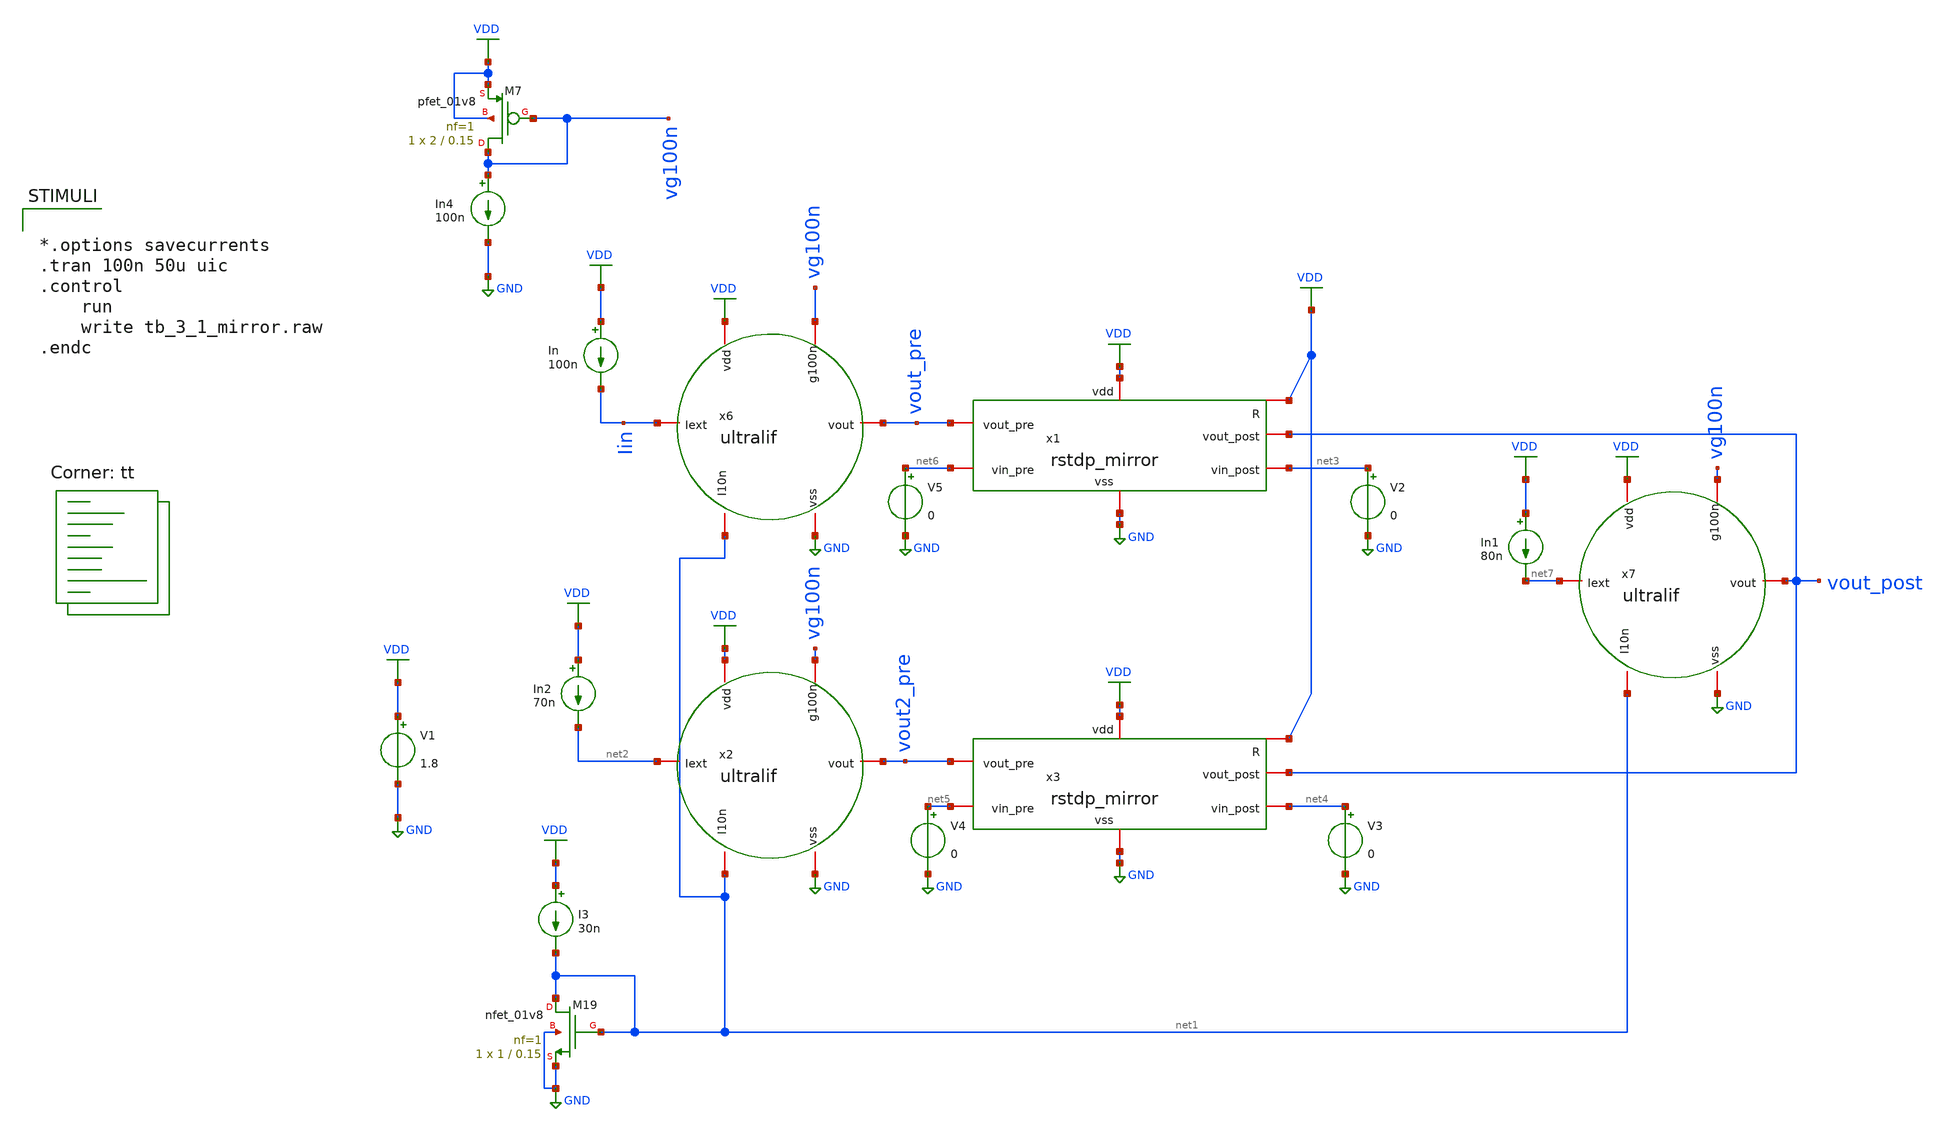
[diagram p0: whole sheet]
** sch_path: tb_3_1_mirror.sch
**.subckt tb_3_1_mirror
V1 VDD GND 1.8
x6 VDD Iin vout_pre net1 GND vg100n ultralif
x7 VDD net7 vout_post net1 GND vg100n ultralif
XM19 net1 net1 GND GND sky130_fd_pr__nfet_01v8 L=0.15 W=1 nf=1 ad='int((nf+1)/2) * W/nf * 0.29' as='int((nf+2)/2) * W/nf * 0.29'
+ pd='2*int((nf+1)/2) * (W/nf + 0.29)' ps='2*int((nf+2)/2) * (W/nf + 0.29)' nrd='0.29 / W' nrs='0.29 / W'
+ sa=0 sb=0 sd=0 mult=1 m=1
I3 VDD net1 30n
In VDD Iin 100n
x2 VDD net2 vout2_pre net1 GND vg100n ultralif
In2 VDD net2 70n
XM7 vg100n vg100n VDD VDD sky130_fd_pr__pfet_01v8 L=0.15 W=2 nf=1 ad='int((nf+1)/2) * W/nf * 0.29' as='int((nf+2)/2) * W/nf * 0.29'
+ pd='2*int((nf+1)/2) * (W/nf + 0.29)' ps='2*int((nf+2)/2) * (W/nf + 0.29)' nrd='0.29 / W' nrs='0.29 / W'
+ sa=0 sb=0 sd=0 mult=1 m=1
In4 vg100n GND 100n
x1 VDD VDD GND vout_pre vout_post net3 net6 rstdp_mirror
x3 VDD VDD GND vout2_pre vout_post net4 net5 rstdp_mirror
V2 net3 GND 0
V3 net4 GND 0
V4 net5 GND 0
V5 net6 GND 0
In1 VDD net7 80n
**** begin user architecture code
.lib $::SKYWATER_MODELS/sky130.lib.spice tt

** opencircuitdesign pdks install
.inc $::SKYWATER_MODELS/rram_v0.spice

**** end user architecture code
**.ends

* expanding   symbol:  /home/alex/Desktop/EDA/SNN_IPN/Neuron/ultralif/ultralif.sym # of pins=6
** sym_path: Neuron/ultralif/ultralif.sym
** sch_path: Neuron/ultralif/ultralif.sch
.subckt ultralif vdd Iext vout I10n vss g100n
*.iopin Iext
*.iopin vout
*.iopin vss
*.iopin I10n
*.iopin vdd
*.iopin g100n
XM1 net2 net2 vm vdd sky130_fd_pr__pfet_01v8 L=10 W=1 nf=1 ad='int((nf+1)/2) * W/nf * 0.29' as='int((nf+2)/2) * W/nf * 0.29'
+ pd='2*int((nf+1)/2) * (W/nf + 0.29)' ps='2*int((nf+2)/2) * (W/nf + 0.29)' nrd='0.29 / W' nrs='0.29 / W'
+ sa=0 sb=0 sd=0 mult=1 m=1
XM2 net2 net1 vm vdd sky130_fd_pr__pfet_01v8 L=0.15 W=1.5 nf=1 ad='int((nf+1)/2) * W/nf * 0.29' as='int((nf+2)/2) * W/nf * 0.29'
+ pd='2*int((nf+1)/2) * (W/nf + 0.29)' ps='2*int((nf+2)/2) * (W/nf + 0.29)' nrd='0.29 / W' nrs='0.29 / W'
+ sa=0 sb=0 sd=0 mult=1 m=1
XM3 net1 net1 vm vdd sky130_fd_pr__pfet_01v8 L=0.15 W=5 nf=1 ad='int((nf+1)/2) * W/nf * 0.29' as='int((nf+2)/2) * W/nf * 0.29'
+ pd='2*int((nf+1)/2) * (W/nf + 0.29)' ps='2*int((nf+2)/2) * (W/nf + 0.29)' nrd='0.29 / W' nrs='0.29 / W'
+ sa=0 sb=0 sd=0 mult=2 m=2
XM4 net1 net2 vss vss sky130_fd_pr__nfet_01v8 L=4 W=1 nf=1 ad='int((1 + 1)/2) * 1 / 1 * 0.29' as='int((1 + 2)/2) * 1 / 1 * 0.29'
+ pd='2*int((1 + 1)/2) * (1 / 1 + 0.29)' ps='2*int((1 + 2)/2) * (1 / 1 + 0.29)' nrd='0.29 / 1 ' nrs='0.29 / 1 '
+ sa=0 sb=0 sd=0 mult=1 m=1
C1 vm vss 0.1p m=1
XM9 vm net2 Iext vdd sky130_fd_pr__pfet_01v8 L=0.15 W=2 nf=1 ad='int((nf+1)/2) * W/nf * 0.29' as='int((nf+2)/2) * W/nf * 0.29'
+ pd='2*int((nf+1)/2) * (W/nf + 0.29)' ps='2*int((nf+2)/2) * (W/nf + 0.29)' nrd='0.29 / W' nrs='0.29 / W'
+ sa=0 sb=0 sd=0 mult=1 m=1
XM10 net2 I10n vss vss sky130_fd_pr__nfet_01v8 L=0.15 W=1 nf=1 ad='int((1 + 1)/2) * 1 / 1 * 0.29' as='int((1 + 2)/2) * 1 / 1 * 0.29'
+ pd='2*int((1 + 1)/2) * (1 / 1 + 0.29)' ps='2*int((1 + 2)/2) * (1 / 1 + 0.29)' nrd='0.29 / 1 ' nrs='0.29 / 1 '
+ sa=0 sb=0 sd=0 mult=1 m=1
XM5 vout net2 vss vss sky130_fd_pr__nfet_01v8 L=0.15 W=1 nf=1 ad='int((1 + 1)/2) * 1 / 1 * 0.29' as='int((1 + 2)/2) * 1 / 1 * 0.29'
+ pd='2*int((1 + 1)/2) * (1 / 1 + 0.29)' ps='2*int((1 + 2)/2) * (1 / 1 + 0.29)' nrd='0.29 / 1 ' nrs='0.29 / 1 '
+ sa=0 sb=0 sd=0 mult=1 m=1
XM6 vout g100n vdd vdd sky130_fd_pr__pfet_01v8 L=0.15 W=2 nf=1 ad='int((nf+1)/2) * W/nf * 0.29' as='int((nf+2)/2) * W/nf * 0.29'
+ pd='2*int((nf+1)/2) * (W/nf + 0.29)' ps='2*int((nf+2)/2) * (W/nf + 0.29)' nrd='0.29 / W' nrs='0.29 / W'
+ sa=0 sb=0 sd=0 mult=1 m=1
.ends


* expanding   symbol:  /home/alex/Desktop/EDA/SNN_IPN/Synapse/rstdp_mirror.sym # of pins=7
** sym_path: Synapse/rstdp_mirror.sym
** sch_path: Synapse/rstdp_mirror.sch
.subckt rstdp_mirror vdd R vss vout_pre vout_post vin_post vin_pre
*.iopin vdd
*.iopin vss
*.iopin R
*.iopin vout_post
*.iopin vout_pre
*.iopin vin_post
*.iopin vin_pre
XR2 te be rram_v0
XM2 net1 R be vss sky130_fd_pr__nfet_01v8 L=0.15 W=7.5 nf=1 ad='int((nf+1)/2) * W/nf * 0.29' as='int((nf+2)/2) * W/nf * 0.29'
+ pd='2*int((nf+1)/2) * (W/nf + 0.29)' ps='2*int((nf+2)/2) * (W/nf + 0.29)' nrd='0.29 / W' nrs='0.29 / W'
+ sa=0 sb=0 sd=0 mult=1 m=1
XM3 te R vpost vss sky130_fd_pr__nfet_01v8 L=0.15 W=7.5 nf=1 ad='int((nf+1)/2) * W/nf * 0.29' as='int((nf+2)/2) * W/nf * 0.29'
+ pd='2*int((nf+1)/2) * (W/nf + 0.29)' ps='2*int((nf+2)/2) * (W/nf + 0.29)' nrd='0.29 / W' nrs='0.29 / W'
+ sa=0 sb=0 sd=0 mult=1 m=1
XM1 te R net1 vdd sky130_fd_pr__pfet_01v8 L=0.15 W=15 nf=1 ad='int((nf+1)/2) * W/nf * 0.29' as='int((nf+2)/2) * W/nf * 0.29'
+ pd='2*int((nf+1)/2) * (W/nf + 0.29)' ps='2*int((nf+2)/2) * (W/nf + 0.29)' nrd='0.29 / W' nrs='0.29 / W'
+ sa=0 sb=0 sd=0 mult=2 m=2
XM4 vpost R be vdd sky130_fd_pr__pfet_01v8 L=0.15 W=15 nf=1 ad='int((nf+1)/2) * W/nf * 0.29' as='int((nf+2)/2) * W/nf * 0.29'
+ pd='2*int((nf+1)/2) * (W/nf + 0.29)' ps='2*int((nf+2)/2) * (W/nf + 0.29)' nrd='0.29 / W' nrs='0.29 / W'
+ sa=0 sb=0 sd=0 mult=2 m=2
XM7 vpost vout_post vss vss sky130_fd_pr__nfet_01v8 L=0.15 W=1 nf=1 ad='int((1 + 1)/2) * 1 / 1 * 0.29'
+ as='int((1 + 2)/2) * 1 / 1 * 0.29' pd='2*int((1 + 1)/2) * (1 / 1 + 0.29)' ps='2*int((1 + 2)/2) * (1 / 1 + 0.29)'
+ nrd='0.29 / 1 ' nrs='0.29 / 1 ' sa=0 sb=0 sd=0 mult=1 m=1
XM5 vpost vout_post vdd vdd sky130_fd_pr__pfet_01v8 L=0.15 W=2 nf=1 ad='int((nf+1)/2) * W/nf * 0.29'
+ as='int((nf+2)/2) * W/nf * 0.29' pd='2*int((nf+1)/2) * (W/nf + 0.29)' ps='2*int((nf+2)/2) * (W/nf + 0.29)'
+ nrd='0.29 / W' nrs='0.29 / W' sa=0 sb=0 sd=0 mult=1 m=1
XM6 vpre vout_pre vss vss sky130_fd_pr__nfet_01v8 L=0.15 W=1 nf=1 ad='int((1 + 1)/2) * 1 / 1 * 0.29'
+ as='int((1 + 2)/2) * 1 / 1 * 0.29' pd='2*int((1 + 1)/2) * (1 / 1 + 0.29)' ps='2*int((1 + 2)/2) * (1 / 1 + 0.29)'
+ nrd='0.29 / 1 ' nrs='0.29 / 1 ' sa=0 sb=0 sd=0 mult=1 m=1
XM8 vpre vout_pre vdd vdd sky130_fd_pr__pfet_01v8 L=0.15 W=2 nf=1 ad='int((nf+1)/2) * W/nf * 0.29' as='int((nf+2)/2) * W/nf * 0.29'
+ pd='2*int((nf+1)/2) * (W/nf + 0.29)' ps='2*int((nf+2)/2) * (W/nf + 0.29)' nrd='0.29 / W' nrs='0.29 / W'
+ sa=0 sb=0 sd=0 mult=1 m=1
XM9 vpre vpre net1 vss sky130_fd_pr__nfet_01v8 L=0.15 W=7.5 nf=1 ad='int((1 + 1)/2) * 7.5 / 1 * 0.29'
+ as='int((1 + 2)/2) * 7.5 / 1 * 0.29' pd='2*int((1 + 1)/2) * (7.5 / 1 + 0.29)' ps='2*int((1 + 2)/2) * (7.5 / 1 + 0.29)'
+ nrd='0.29 / 7.5 ' nrs='0.29 / 7.5 ' sa=0 sb=0 sd=0 mult=1 m=1
XM10 vdd vpre vin_post vss sky130_fd_pr__nfet_01v8 L=0.15 W=1 nf=1 ad='int((1 + 1)/2) * 1 / 1 * 0.29'
+ as='int((1 + 2)/2) * 1 / 1 * 0.29' pd='2*int((1 + 1)/2) * (1 / 1 + 0.29)' ps='2*int((1 + 2)/2) * (1 / 1 + 0.29)'
+ nrd='0.29 / 1 ' nrs='0.29 / 1 ' sa=0 sb=0 sd=0 mult=1 m=1
XM11 net1 net1 vpre vss sky130_fd_pr__nfet_01v8 L=0.15 W=7.5 nf=1 ad='int((1 + 1)/2) * 7.5 / 1 * 0.29'
+ as='int((1 + 2)/2) * 7.5 / 1 * 0.29' pd='2*int((1 + 1)/2) * (7.5 / 1 + 0.29)' ps='2*int((1 + 2)/2) * (7.5 / 1 + 0.29)'
+ nrd='0.29 / 7.5 ' nrs='0.29 / 7.5 ' sa=0 sb=0 sd=0 mult=1 m=1
XM12 vdd net1 vin_pre vss sky130_fd_pr__nfet_01v8 L=0.15 W=7.5 nf=1 ad='int((1 + 1)/2) * 7.5 / 1 * 0.29'
+ as='int((1 + 2)/2) * 7.5 / 1 * 0.29' pd='2*int((1 + 1)/2) * (7.5 / 1 + 0.29)' ps='2*int((1 + 2)/2) * (7.5 / 1 + 0.29)'
+ nrd='0.29 / 7.5 ' nrs='0.29 / 7.5 ' sa=0 sb=0 sd=0 mult=1 m=1
.ends

.GLOBAL VDD
.GLOBAL GND
**** begin user architecture code


*.options savecurrents
.tran 100n 50u uic
.control
	run
	write tb_3_1_mirror.raw
.endc


**** end user architecture code
.end
